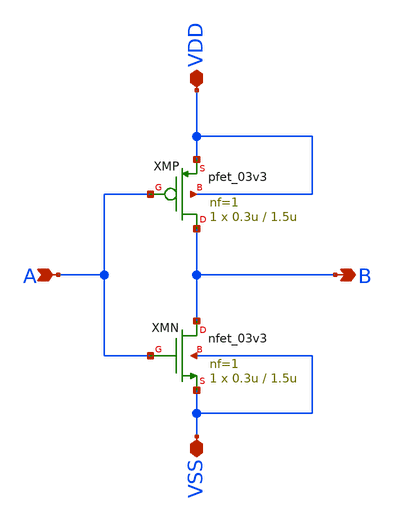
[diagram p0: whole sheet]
** sch_path: designs/gate_inv_x1/edge_detector_inv.sch
**.subckt edge_detector_inv B A VDD VSS
*.opin B
*.ipin A
*.iopin VDD
*.iopin VSS
XMN B A VSS VSS nfet_03v3 L=1.5u W=0.3u nf=1 ad='int((nf+1)/2) * W/nf * 0.18u' as='int((nf+2)/2) * W/nf * 0.18u'
+ pd='2*int((nf+1)/2) * (W/nf + 0.18u)' ps='2*int((nf+2)/2) * (W/nf + 0.18u)' nrd='0.18u / W' nrs='0.18u / W'
+ sa=0 sb=0 sd=0 m=1
XMP B A VDD VDD pfet_03v3 L=1.5u W=0.3u nf=1 ad='int((nf+1)/2) * W/nf * 0.18u' as='int((nf+2)/2) * W/nf * 0.18u'
+ pd='2*int((nf+1)/2) * (W/nf + 0.18u)' ps='2*int((nf+2)/2) * (W/nf + 0.18u)' nrd='0.18u / W' nrs='0.18u / W'
+ sa=0 sb=0 sd=0 m=1
**.ends
.end
